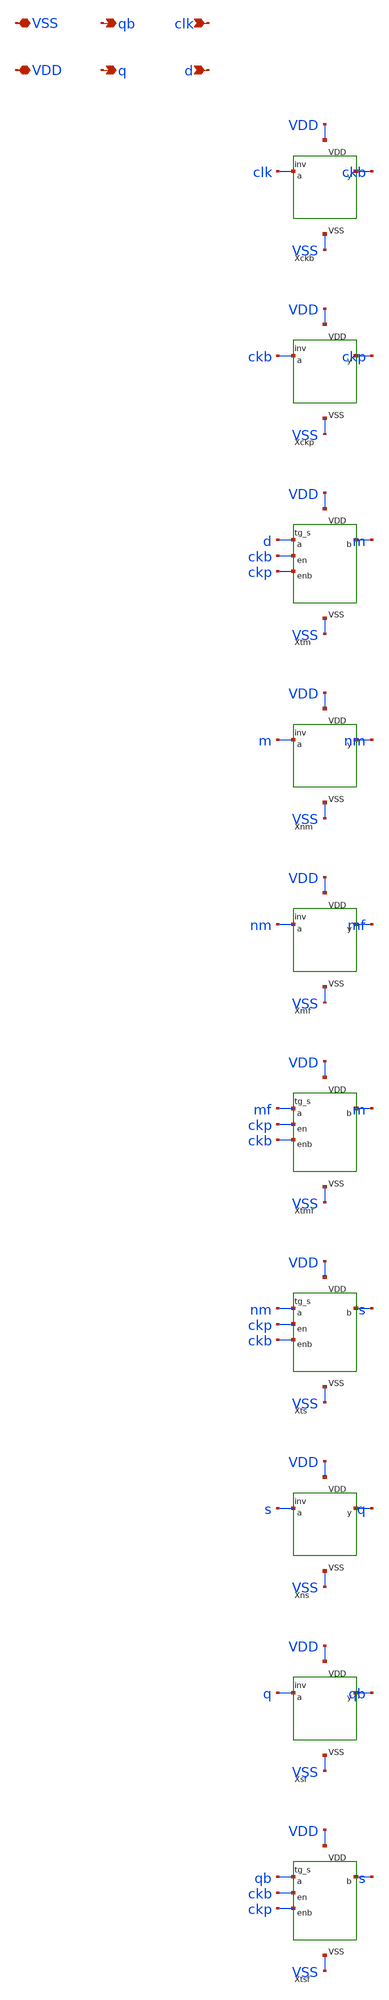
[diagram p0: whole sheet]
** sch_path: design/dff.sch
**.subckt dff d clk q qb VDD VSS
*.ipin d
*.ipin clk
*.opin q
*.opin qb
*.iopin VDD
*.iopin VSS
XXckb clk ckb VDD VSS inv
XXckp ckb ckp VDD VSS inv
XXtm d ckb ckp m VDD VSS tg_s
XXnm m nm VDD VSS inv
XXmf nm mf VDD VSS inv
XXtmf mf ckp ckb m VDD VSS tg_s
XXts nm ckp ckb s VDD VSS tg_s
XXns s q VDD VSS inv
XXsf q qb VDD VSS inv
XXtsf qb ckb ckp s VDD VSS tg_s
**.ends

* expanding   symbol:  inv.sym # of pins=4
** sym_path: design/inv.sym
** sch_path: design/inv.sch
.subckt inv a y VDD VSS

*.ipin a
*.opin y
*.iopin VDD
*.iopin VSS
XMP y a VDD VDD pfet_03v3 L=0.28u W=1u nf=1 ad='int((nf+1)/2) * W/nf * 0.18u' as='int((nf+2)/2) * W/nf * 0.18u'
+ pd='2*int((nf+1)/2) * (W/nf + 0.18u)' ps='2*int((nf+2)/2) * (W/nf + 0.18u)' nrd='0.18u / W' nrs='0.18u / W'
+ sa=0 sb=0 sd=0 m=1
XMN y a VSS VSS nfet_03v3 L=0.28u W=0.5u nf=1 ad='int((nf+1)/2) * W/nf * 0.18u' as='int((nf+2)/2) * W/nf * 0.18u'
+ pd='2*int((nf+1)/2) * (W/nf + 0.18u)' ps='2*int((nf+2)/2) * (W/nf + 0.18u)' nrd='0.18u / W' nrs='0.18u / W'
+ sa=0 sb=0 sd=0 m=1
.ends


* expanding   symbol:  tg_s.sym # of pins=6
** sym_path: design/tg_s.sym
** sch_path: design/tg_s.sch
.subckt tg_s a en enb b VDD VSS

*.ipin a
*.ipin en
*.ipin enb
*.iopin b
*.iopin VDD
*.iopin VSS
XMN a en b VSS nfet_03v3 L=0.28u W=0.5u nf=1 ad='int((nf+1)/2) * W/nf * 0.18u' as='int((nf+2)/2) * W/nf * 0.18u'
+ pd='2*int((nf+1)/2) * (W/nf + 0.18u)' ps='2*int((nf+2)/2) * (W/nf + 0.18u)' nrd='0.18u / W' nrs='0.18u / W'
+ sa=0 sb=0 sd=0 m=1
XMP a enb b VDD pfet_03v3 L=0.28u W=1u nf=1 ad='int((nf+1)/2) * W/nf * 0.18u' as='int((nf+2)/2) * W/nf * 0.18u'
+ pd='2*int((nf+1)/2) * (W/nf + 0.18u)' ps='2*int((nf+2)/2) * (W/nf + 0.18u)' nrd='0.18u / W' nrs='0.18u / W'
+ sa=0 sb=0 sd=0 m=1
.ends

.end
